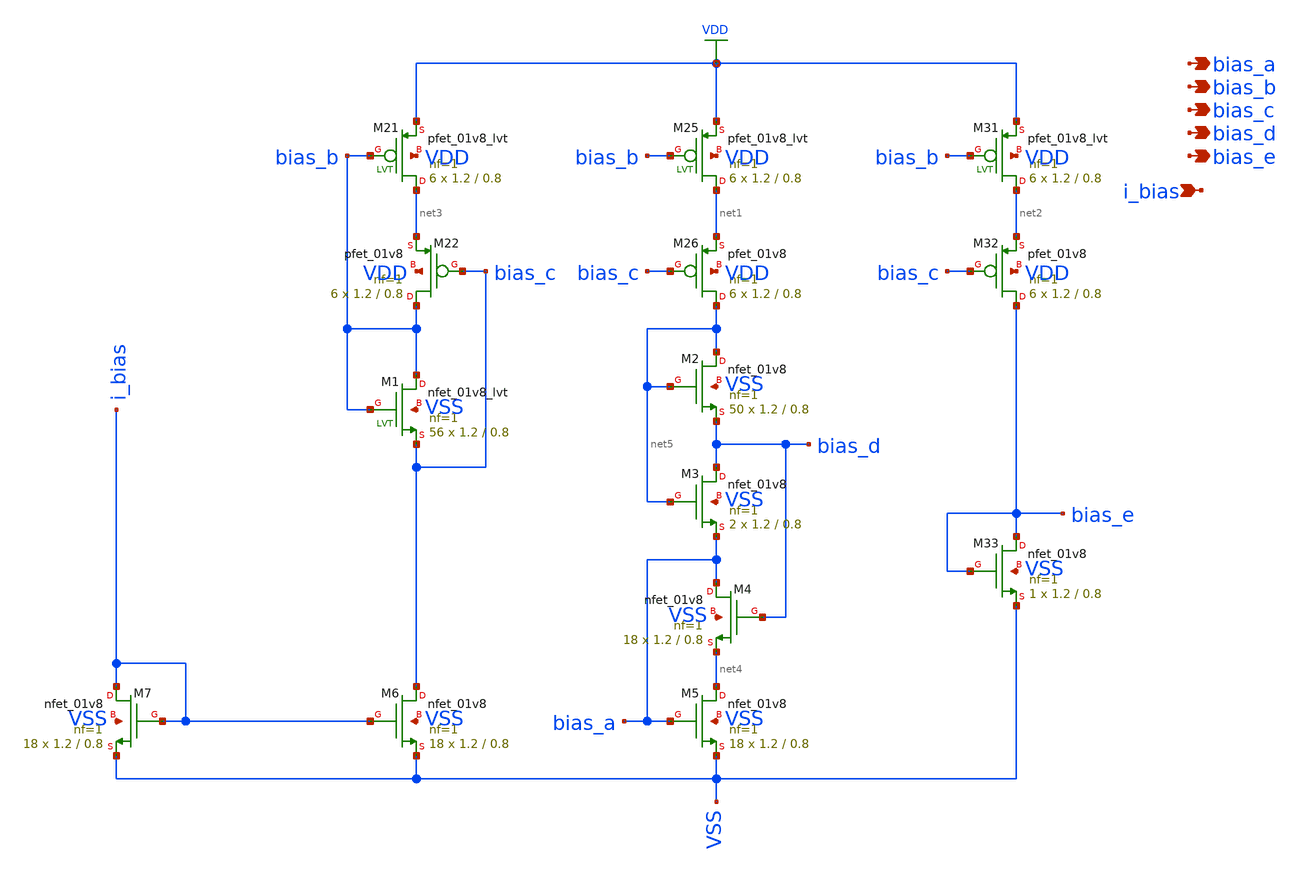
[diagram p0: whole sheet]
** sch_path: design/analog_modulator/schematic/folded_cascode_2_bias.sch
**.subckt folded_cascode_2_bias bias_a bias_b bias_c bias_d bias_e i_bias
*.opin bias_a
*.opin bias_b
*.opin bias_c
*.opin bias_d
*.opin bias_e
*.ipin i_bias
XM22 bias_b bias_c net3 VDD sky130_fd_pr__pfet_01v8 L=0.8 W=1.2 nf=1 ad='int((nf+1)/2) * W/nf * 0.29'
+ as='int((nf+2)/2) * W/nf * 0.29' pd='2*int((nf+1)/2) * (W/nf + 0.29)' ps='2*int((nf+2)/2) * (W/nf + 0.29)'
+ nrd='0.29 / W' nrs='0.29 / W' sa=0 sb=0 sd=0 mult=6 m=6
XM26 net5 bias_c net1 VDD sky130_fd_pr__pfet_01v8 L=0.8 W=1.2 nf=1 ad='int((nf+1)/2) * W/nf * 0.29' as='int((nf+2)/2) * W/nf * 0.29'
+ pd='2*int((nf+1)/2) * (W/nf + 0.29)' ps='2*int((nf+2)/2) * (W/nf + 0.29)' nrd='0.29 / W' nrs='0.29 / W'
+ sa=0 sb=0 sd=0 mult=6 m=6
XM32 bias_e bias_c net2 VDD sky130_fd_pr__pfet_01v8 L=0.8 W=1.2 nf=1 ad='int((nf+1)/2) * W/nf * 0.29'
+ as='int((nf+2)/2) * W/nf * 0.29' pd='2*int((nf+1)/2) * (W/nf + 0.29)' ps='2*int((nf+2)/2) * (W/nf + 0.29)'
+ nrd='0.29 / W' nrs='0.29 / W' sa=0 sb=0 sd=0 mult=6 m=6
XM33 bias_e bias_e VSS VSS sky130_fd_pr__nfet_01v8 L=0.8 W=1.2 nf=1 ad='int((nf+1)/2) * W/nf * 0.29'
+ as='int((nf+2)/2) * W/nf * 0.29' pd='2*int((nf+1)/2) * (W/nf + 0.29)' ps='2*int((nf+2)/2) * (W/nf + 0.29)'
+ nrd='0.29 / W' nrs='0.29 / W' sa=0 sb=0 sd=0 mult=1 m=1
XM21 net3 bias_b VDD VDD sky130_fd_pr__pfet_01v8_lvt L=0.8 W=1.2 nf=1 ad='int((nf+1)/2) * W/nf * 0.29'
+ as='int((nf+2)/2) * W/nf * 0.29' pd='2*int((nf+1)/2) * (W/nf + 0.29)' ps='2*int((nf+2)/2) * (W/nf + 0.29)'
+ nrd='0.29 / W' nrs='0.29 / W' sa=0 sb=0 sd=0 mult=6 m=6
XM25 net1 bias_b VDD VDD sky130_fd_pr__pfet_01v8_lvt L=0.8 W=1.2 nf=1 ad='int((nf+1)/2) * W/nf * 0.29'
+ as='int((nf+2)/2) * W/nf * 0.29' pd='2*int((nf+1)/2) * (W/nf + 0.29)' ps='2*int((nf+2)/2) * (W/nf + 0.29)'
+ nrd='0.29 / W' nrs='0.29 / W' sa=0 sb=0 sd=0 mult=6 m=6
XM31 net2 bias_b VDD VDD sky130_fd_pr__pfet_01v8_lvt L=0.8 W=1.2 nf=1 ad='int((nf+1)/2) * W/nf * 0.29'
+ as='int((nf+2)/2) * W/nf * 0.29' pd='2*int((nf+1)/2) * (W/nf + 0.29)' ps='2*int((nf+2)/2) * (W/nf + 0.29)'
+ nrd='0.29 / W' nrs='0.29 / W' sa=0 sb=0 sd=0 mult=6 m=6
XM1 bias_b bias_b bias_c VSS sky130_fd_pr__nfet_01v8_lvt L=0.8 W=1.2 nf=1 ad='int((nf+1)/2) * W/nf * 0.29'
+ as='int((nf+2)/2) * W/nf * 0.29' pd='2*int((nf+1)/2) * (W/nf + 0.29)' ps='2*int((nf+2)/2) * (W/nf + 0.29)'
+ nrd='0.29 / W' nrs='0.29 / W' sa=0 sb=0 sd=0 mult=56 m=56
XM2 net5 net5 bias_d VSS sky130_fd_pr__nfet_01v8 L=0.8 W=1.2 nf=1 ad='int((nf+1)/2) * W/nf * 0.29' as='int((nf+2)/2) * W/nf * 0.29'
+ pd='2*int((nf+1)/2) * (W/nf + 0.29)' ps='2*int((nf+2)/2) * (W/nf + 0.29)' nrd='0.29 / W' nrs='0.29 / W'
+ sa=0 sb=0 sd=0 mult=50 m=50
XM3 bias_d net5 bias_a VSS sky130_fd_pr__nfet_01v8 L=0.8 W=1.2 nf=1 ad='int((nf+1)/2) * W/nf * 0.29'
+ as='int((nf+2)/2) * W/nf * 0.29' pd='2*int((nf+1)/2) * (W/nf + 0.29)' ps='2*int((nf+2)/2) * (W/nf + 0.29)'
+ nrd='0.29 / W' nrs='0.29 / W' sa=0 sb=0 sd=0 mult=2 m=2
XM4 bias_a bias_d net4 VSS sky130_fd_pr__nfet_01v8 L=0.8 W=1.2 nf=1 ad='int((nf+1)/2) * W/nf * 0.29'
+ as='int((nf+2)/2) * W/nf * 0.29' pd='2*int((nf+1)/2) * (W/nf + 0.29)' ps='2*int((nf+2)/2) * (W/nf + 0.29)'
+ nrd='0.29 / W' nrs='0.29 / W' sa=0 sb=0 sd=0 mult=18 m=18
XM5 net4 bias_a VSS VSS sky130_fd_pr__nfet_01v8 L=0.8 W=1.2 nf=1 ad='int((nf+1)/2) * W/nf * 0.29' as='int((nf+2)/2) * W/nf * 0.29'
+ pd='2*int((nf+1)/2) * (W/nf + 0.29)' ps='2*int((nf+2)/2) * (W/nf + 0.29)' nrd='0.29 / W' nrs='0.29 / W'
+ sa=0 sb=0 sd=0 mult=18 m=18
XM6 bias_c i_bias VSS VSS sky130_fd_pr__nfet_01v8 L=0.8 W=1.2 nf=1 ad='int((nf+1)/2) * W/nf * 0.29' as='int((nf+2)/2) * W/nf * 0.29'
+ pd='2*int((nf+1)/2) * (W/nf + 0.29)' ps='2*int((nf+2)/2) * (W/nf + 0.29)' nrd='0.29 / W' nrs='0.29 / W'
+ sa=0 sb=0 sd=0 mult=18 m=18
XM7 i_bias i_bias VSS VSS sky130_fd_pr__nfet_01v8 L=0.8 W=1.2 nf=1 ad='int((nf+1)/2) * W/nf * 0.29' as='int((nf+2)/2) * W/nf * 0.29'
+ pd='2*int((nf+1)/2) * (W/nf + 0.29)' ps='2*int((nf+2)/2) * (W/nf + 0.29)' nrd='0.29 / W' nrs='0.29 / W'
+ sa=0 sb=0 sd=0 mult=18 m=18
**.ends
.GLOBAL VDD
.end
